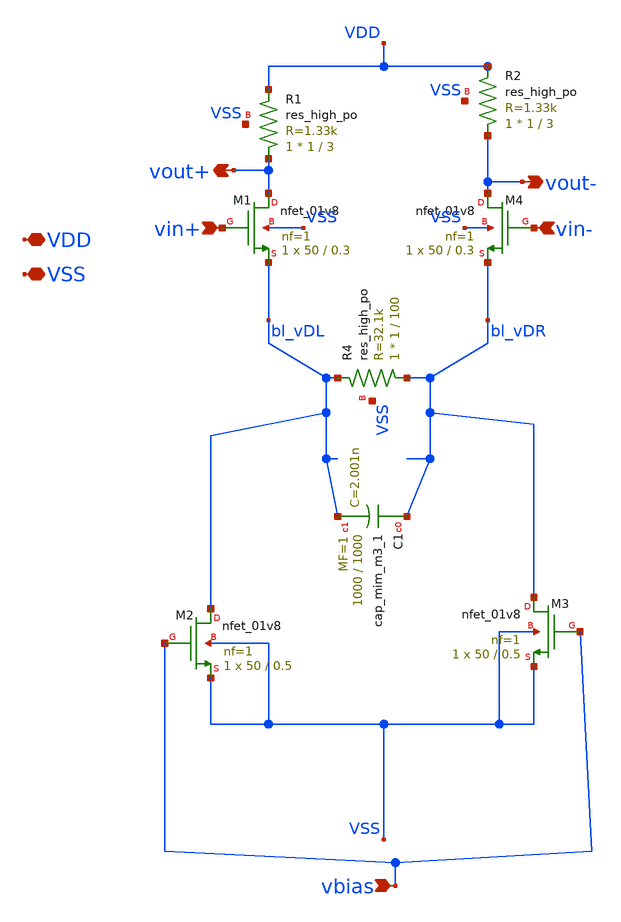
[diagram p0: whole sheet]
** sch_path: xschem/CTLE.sch
**.subckt CTLE VDD VSS vin+ vin- vout- vout+ vbias
*.iopin VDD
*.iopin VSS
*.ipin vin+
*.ipin vin-
*.opin vout-
*.opin vout+
*.ipin vbias
XM1 vout+ vin+ bl_vDL VSS sky130_fd_pr__nfet_01v8 L=0.3 W=50 nf=1 ad='int((nf+1)/2) * W/nf * 0.29' as='int((nf+2)/2) * W/nf * 0.29'
+ pd='2*int((nf+1)/2) * (W/nf + 0.29)' ps='2*int((nf+2)/2) * (W/nf + 0.29)' nrd='0.29 / W' nrs='0.29 / W'
+ sa=0 sb=0 sd=0 mult=1 m=1
XM2 bl_vDL vbias VSS VSS sky130_fd_pr__nfet_01v8 L=0.5 W=50 nf=1 ad='int((nf+1)/2) * W/nf * 0.29' as='int((nf+2)/2) * W/nf * 0.29'
+ pd='2*int((nf+1)/2) * (W/nf + 0.29)' ps='2*int((nf+2)/2) * (W/nf + 0.29)' nrd='0.29 / W' nrs='0.29 / W'
+ sa=0 sb=0 sd=0 mult=1 m=1
XM4 vout- vin- bl_vDR VSS sky130_fd_pr__nfet_01v8 L=0.3 W=50 nf=1 ad='int((nf+1)/2) * W/nf * 0.29' as='int((nf+2)/2) * W/nf * 0.29'
+ pd='2*int((nf+1)/2) * (W/nf + 0.29)' ps='2*int((nf+2)/2) * (W/nf + 0.29)' nrd='0.29 / W' nrs='0.29 / W'
+ sa=0 sb=0 sd=0 mult=1 m=1
XR1 vout+ VDD VSS sky130_fd_pr__res_high_po W=1 L=3 mult=1 m=1
XR2 vout- VDD VSS sky130_fd_pr__res_high_po W=1 L=3 mult=1 m=1
XR4 bl_vDR bl_vDL VSS sky130_fd_pr__res_high_po W=1 L=100 mult=1 m=1
XC1 bl_vDR bl_vDL sky130_fd_pr__cap_mim_m3_1 W=1000 L=1000 MF=1 m=1
XM3 bl_vDR vbias VSS VSS sky130_fd_pr__nfet_01v8 L=0.5 W=50 nf=1 ad='int((nf+1)/2) * W/nf * 0.29' as='int((nf+2)/2) * W/nf * 0.29'
+ pd='2*int((nf+1)/2) * (W/nf + 0.29)' ps='2*int((nf+2)/2) * (W/nf + 0.29)' nrd='0.29 / W' nrs='0.29 / W'
+ sa=0 sb=0 sd=0 mult=1 m=1
**.ends
.end
